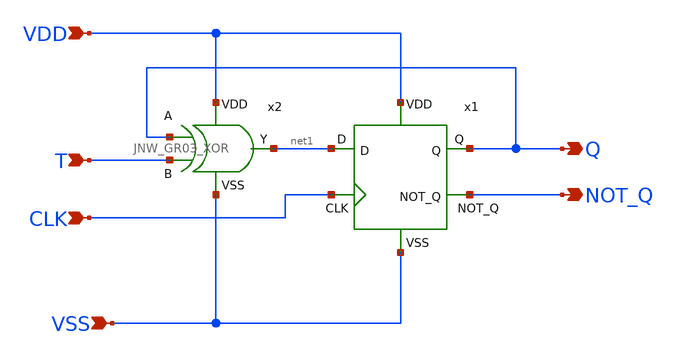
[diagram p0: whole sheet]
** sch_path: design/JNW_GR03_SKY130A/JNW_GR03_TFLIPFLOP_R.sch
**.subckt JNW_GR03_TFLIPFLOP_R VDD Q VSS CLK T NOT_Q
*.ipin VDD
*.opin Q
*.ipin VSS
*.ipin CLK
*.ipin T
*.opin NOT_Q
x1 VDD Q net1 NOT_Q CLK VSS JNW_GR03_DFLIPFLOP_R
x2 VDD Q net1 T VSS JNW_GR03_XOR
**.ends
.end
